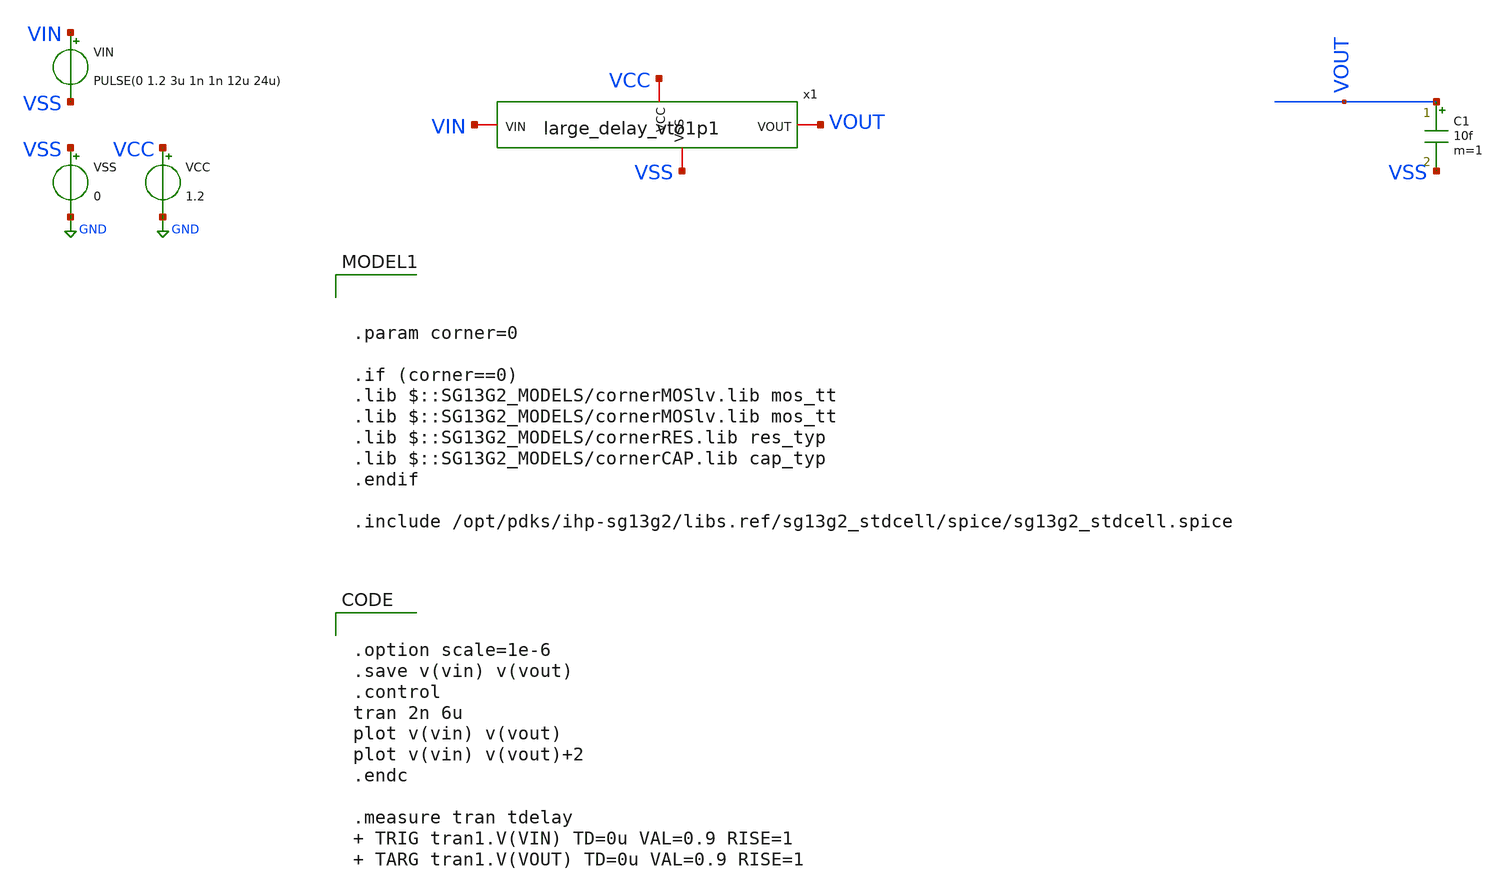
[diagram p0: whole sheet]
** sch_path: xschem/large_delay/tb_largedelay_vto1p1.sch
**.subckt tb_largedelay_vto1p1
VCC VCC GND 1.2
VSS VSS GND 0
VIN VIN VSS PULSE(0 1.2 3u 1n 1n 12u 24u)
C1 VOUT VSS 10f m=1
x1 VCC VSS VIN VOUT large_delay_vto1p1
**** begin user architecture code


.option scale=1e-6
.save v(vin) v(vout)
.control
tran 2n 6u
plot v(vin) v(vout)
plot v(vin) v(vout)+2
.endc

.measure tran tdelay  TRIG tran1.V(VIN) TD=0u VAL=0.9 RISE=1  TARG tran1.V(VOUT) TD=0u VAL=0.9
+ RISE=1






.param corner=0

.if (corner==0)
.lib $::SG13G2_MODELS/cornerMOSlv.lib mos_tt
.lib $::SG13G2_MODELS/cornerMOSlv.lib mos_tt
.lib $::SG13G2_MODELS/cornerRES.lib res_typ
.lib $::SG13G2_MODELS/cornerCAP.lib cap_typ
.endif

.include /opt/pdks/ihp-sg13g2/libs.ref/sg13g2_stdcell/spice/sg13g2_stdcell.spice

**** end user architecture code
**.ends

* expanding   symbol:  large_delay_vto1p1.sym # of pins=4
** sym_path: xschem/large_delay/large_delay_vto1p1.sym
** sch_path: xschem/large_delay/large_delay_vto1p1.sch
.subckt large_delay_vto1p1 VCC VSS VIN VOUT
*.iopin VIN
*.iopin VOUT
*.iopin VCC
*.iopin VSS
x1[0] n2 VIN VCC VSS sg13g2_dlygate4sd3_1
x1[1] n3 n2 VCC VSS sg13g2_dlygate4sd3_1
x1[2] n4 n3 VCC VSS sg13g2_dlygate4sd3_1
x1[3] n5 n4 VCC VSS sg13g2_dlygate4sd3_1
x1[4] VOUT n5 VCC VSS sg13g2_dlygate4sd3_1
.ends


* expanding   symbol:  sg13g2_stdcells/sg13g2_dlygate4sd3_1.sym # of pins=2
** sym_path: sg13g2_stdcells/sg13g2_dlygate4sd3_1.sym
** sch_path: sg13g2_stdcells/sg13g2_dlygate4sd3_1.sch
.subckt sg13g2_dlygate4sd3_1 X A VDD VSS
*.ipin A
*.opin X
*.iopin VDD
*.iopin VSS
XM1 net3 A VSS VSS sg13_lv_nmos w=420.00n l=130.00n ng=1 m=1 mm_ok=1
XM2 net1 net3 VSS VSS sg13_lv_nmos w=420.00n l=500.0n ng=1 m=1 mm_ok=1
XM3 net2 net1 VSS VSS sg13_lv_nmos w=420.00n l=500.0n ng=1 m=1 mm_ok=1
XM4 X net2 VSS VSS sg13_lv_nmos w=740.00n l=130.00n ng=1 m=1 mm_ok=1
XM5 net3 A VDD VDD sg13_lv_pmos w=420.00n l=130.00n ng=1 m=1 mm_ok=1
XM6 net1 net3 VDD VDD sg13_lv_pmos w=1.000u l=500.0n ng=1 m=1 mm_ok=1
XM7 net2 net1 VDD VDD sg13_lv_pmos w=1.000u l=500.0n ng=1 m=1 mm_ok=1
XM8 X net2 VDD VDD sg13_lv_pmos w=1.12u l=130.00n ng=1 m=1 mm_ok=1
.ends

.GLOBAL GND
.end
